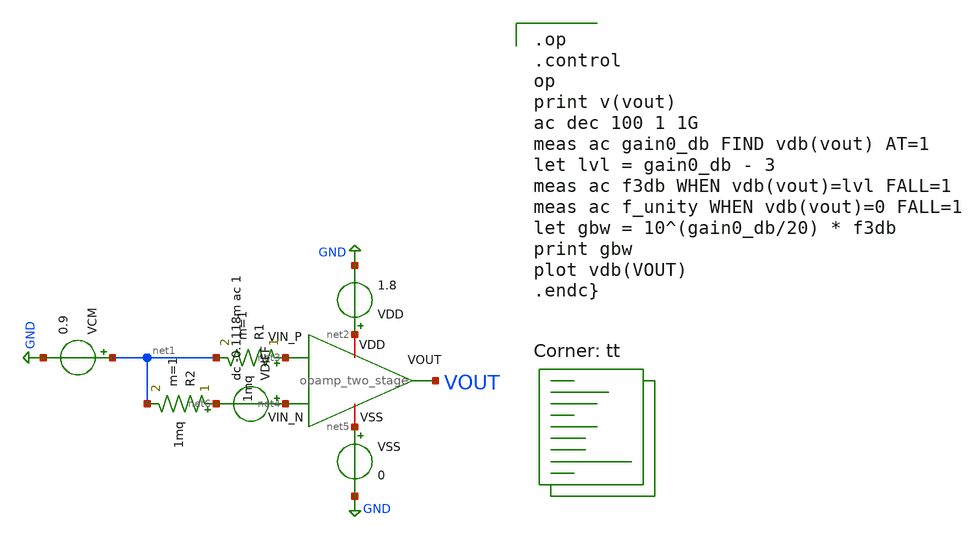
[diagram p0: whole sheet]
** sch_path: analog/bootcamp_opamp/schematics/tb_ac_analysis.sch
**.subckt tb_ac_analysis
x1 net2 VOUT net3 net4 net5 opamp_two_stage
VSS net5 GND 0
VDD net2 GND 1.8
VCM net1 GND 0.9
VDIFF net4 net6 dc -0.1118m ac 1
R1 net3 net1 1mq m=1
R2 net6 net1 1mq m=1
**** begin user architecture code

.op
.control
op
print v(vout)
ac dec 100 1 1G
meas ac gain0_db FIND vdb(vout) AT=1
let lvl = gain0_db - 3
meas ac f3db WHEN vdb(vout)=lvl FALL=1
meas ac f_unity WHEN vdb(vout)=0 FALL=1
let gbw = 10^(gain0_db/20) * f3db
print gbw
plot vdb(VOUT)
.endc}

.lib $::SKYWATER_MODELS/sky130.lib.spice tt
**** end user architecture code
**.ends
.GLOBAL GND
.end
